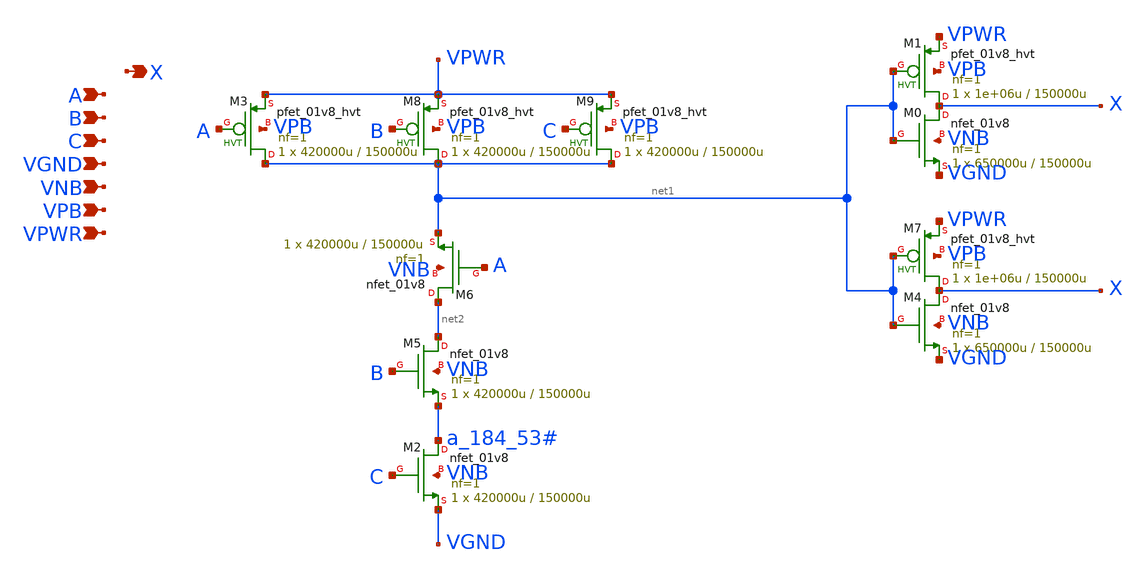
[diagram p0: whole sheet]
** sch_path: schematics/and3/sky130_fd_sc_hd__and3_2.sch
**.subckt sky130_fd_sc_hd__and3_2 A B C VGND VNB VPB VPWR X
*.ipin A
*.ipin B
*.ipin C
*.ipin VGND
*.ipin VNB
*.ipin VPB
*.ipin VPWR
*.opin X
XM1 X net1 VPWR VPB sky130_fd_pr__pfet_01v8_hvt L=150000u W=1e+06u nf=1 ad='int((1 + 1)/2) * 1e+06u / 1 * 0.29'
+ as='int((1 + 2)/2) * 1e+06u / 1 * 0.29' pd='2*int((1 + 1)/2) * (1e+06u / 1 + 0.29)' ps='2*int((1 + 2)/2) * (1e+06u / 1 + 0.29)'
+ nrd='0.29 / 1e+06u ' nrs='0.29 / 1e+06u ' sa=0 sb=0 sd=0 mult=1 m=1
XM0 X net1 VGND VNB sky130_fd_pr__nfet_01v8 L=150000u W=650000u nf=1 ad='int((1 + 1)/2) * 650000u / 1 * 0.29'
+ as='int((1 + 2)/2) * 650000u / 1 * 0.29' pd='2*int((1 + 1)/2) * (650000u / 1 + 0.29)' ps='2*int((1 + 2)/2) * (650000u / 1 + 0.29)'
+ nrd='0.29 / 650000u ' nrs='0.29 / 650000u ' sa=0 sb=0 sd=0 mult=1 m=1
XM7 X net1 VPWR VPB sky130_fd_pr__pfet_01v8_hvt L=150000u W=1e+06u nf=1 ad='int((1 + 1)/2) * 1e+06u / 1 * 0.29'
+ as='int((1 + 2)/2) * 1e+06u / 1 * 0.29' pd='2*int((1 + 1)/2) * (1e+06u / 1 + 0.29)' ps='2*int((1 + 2)/2) * (1e+06u / 1 + 0.29)'
+ nrd='0.29 / 1e+06u ' nrs='0.29 / 1e+06u ' sa=0 sb=0 sd=0 mult=1 m=1
XM4 X net1 VGND VNB sky130_fd_pr__nfet_01v8 L=150000u W=650000u nf=1 ad='int((1 + 1)/2) * 650000u / 1 * 0.29'
+ as='int((1 + 2)/2) * 650000u / 1 * 0.29' pd='2*int((1 + 1)/2) * (650000u / 1 + 0.29)' ps='2*int((1 + 2)/2) * (650000u / 1 + 0.29)'
+ nrd='0.29 / 650000u ' nrs='0.29 / 650000u ' sa=0 sb=0 sd=0 mult=1 m=1
XM3 net1 A VPWR VPB sky130_fd_pr__pfet_01v8_hvt L=150000u W=420000u nf=1 ad='int((1 + 1)/2) * 420000u / 1 * 0.29'
+ as='int((1 + 2)/2) * 420000u / 1 * 0.29' pd='2*int((1 + 1)/2) * (420000u / 1 + 0.29)' ps='2*int((1 + 2)/2) * (420000u / 1 + 0.29)'
+ nrd='0.29 / 420000u ' nrs='0.29 / 420000u ' sa=0 sb=0 sd=0 mult=1 m=1
XM8 net1 B VPWR VPB sky130_fd_pr__pfet_01v8_hvt L=150000u W=420000u nf=1 ad='int((1 + 1)/2) * 420000u / 1 * 0.29'
+ as='int((1 + 2)/2) * 420000u / 1 * 0.29' pd='2*int((1 + 1)/2) * (420000u / 1 + 0.29)' ps='2*int((1 + 2)/2) * (420000u / 1 + 0.29)'
+ nrd='0.29 / 420000u ' nrs='0.29 / 420000u ' sa=0 sb=0 sd=0 mult=1 m=1
XM9 net1 C VPWR VPB sky130_fd_pr__pfet_01v8_hvt L=150000u W=420000u nf=1 ad='int((1 + 1)/2) * 420000u / 1 * 0.29'
+ as='int((1 + 2)/2) * 420000u / 1 * 0.29' pd='2*int((1 + 1)/2) * (420000u / 1 + 0.29)' ps='2*int((1 + 2)/2) * (420000u / 1 + 0.29)'
+ nrd='0.29 / 420000u ' nrs='0.29 / 420000u ' sa=0 sb=0 sd=0 mult=1 m=1
XM6 net2 A net1 VNB sky130_fd_pr__nfet_01v8 L=150000u W=420000u nf=1 ad='int((1 + 1)/2) * 420000u / 1 * 0.29'
+ as='int((1 + 2)/2) * 420000u / 1 * 0.29' pd='2*int((1 + 1)/2) * (420000u / 1 + 0.29)' ps='2*int((1 + 2)/2) * (420000u / 1 + 0.29)'
+ nrd='0.29 / 420000u ' nrs='0.29 / 420000u ' sa=0 sb=0 sd=0 mult=1 m=1
XM5 net2 B a_184_53# VNB sky130_fd_pr__nfet_01v8 L=150000u W=420000u nf=1 ad='int((1 + 1)/2) * 420000u / 1 * 0.29'
+ as='int((1 + 2)/2) * 420000u / 1 * 0.29' pd='2*int((1 + 1)/2) * (420000u / 1 + 0.29)' ps='2*int((1 + 2)/2) * (420000u / 1 + 0.29)'
+ nrd='0.29 / 420000u ' nrs='0.29 / 420000u ' sa=0 sb=0 sd=0 mult=1 m=1
XM2 a_184_53# C VGND VNB sky130_fd_pr__nfet_01v8 L=150000u W=420000u nf=1 ad='int((1 + 1)/2) * 420000u / 1 * 0.29'
+ as='int((1 + 2)/2) * 420000u / 1 * 0.29' pd='2*int((1 + 1)/2) * (420000u / 1 + 0.29)' ps='2*int((1 + 2)/2) * (420000u / 1 + 0.29)'
+ nrd='0.29 / 420000u ' nrs='0.29 / 420000u ' sa=0 sb=0 sd=0 mult=1 m=1
**.ends
.end
